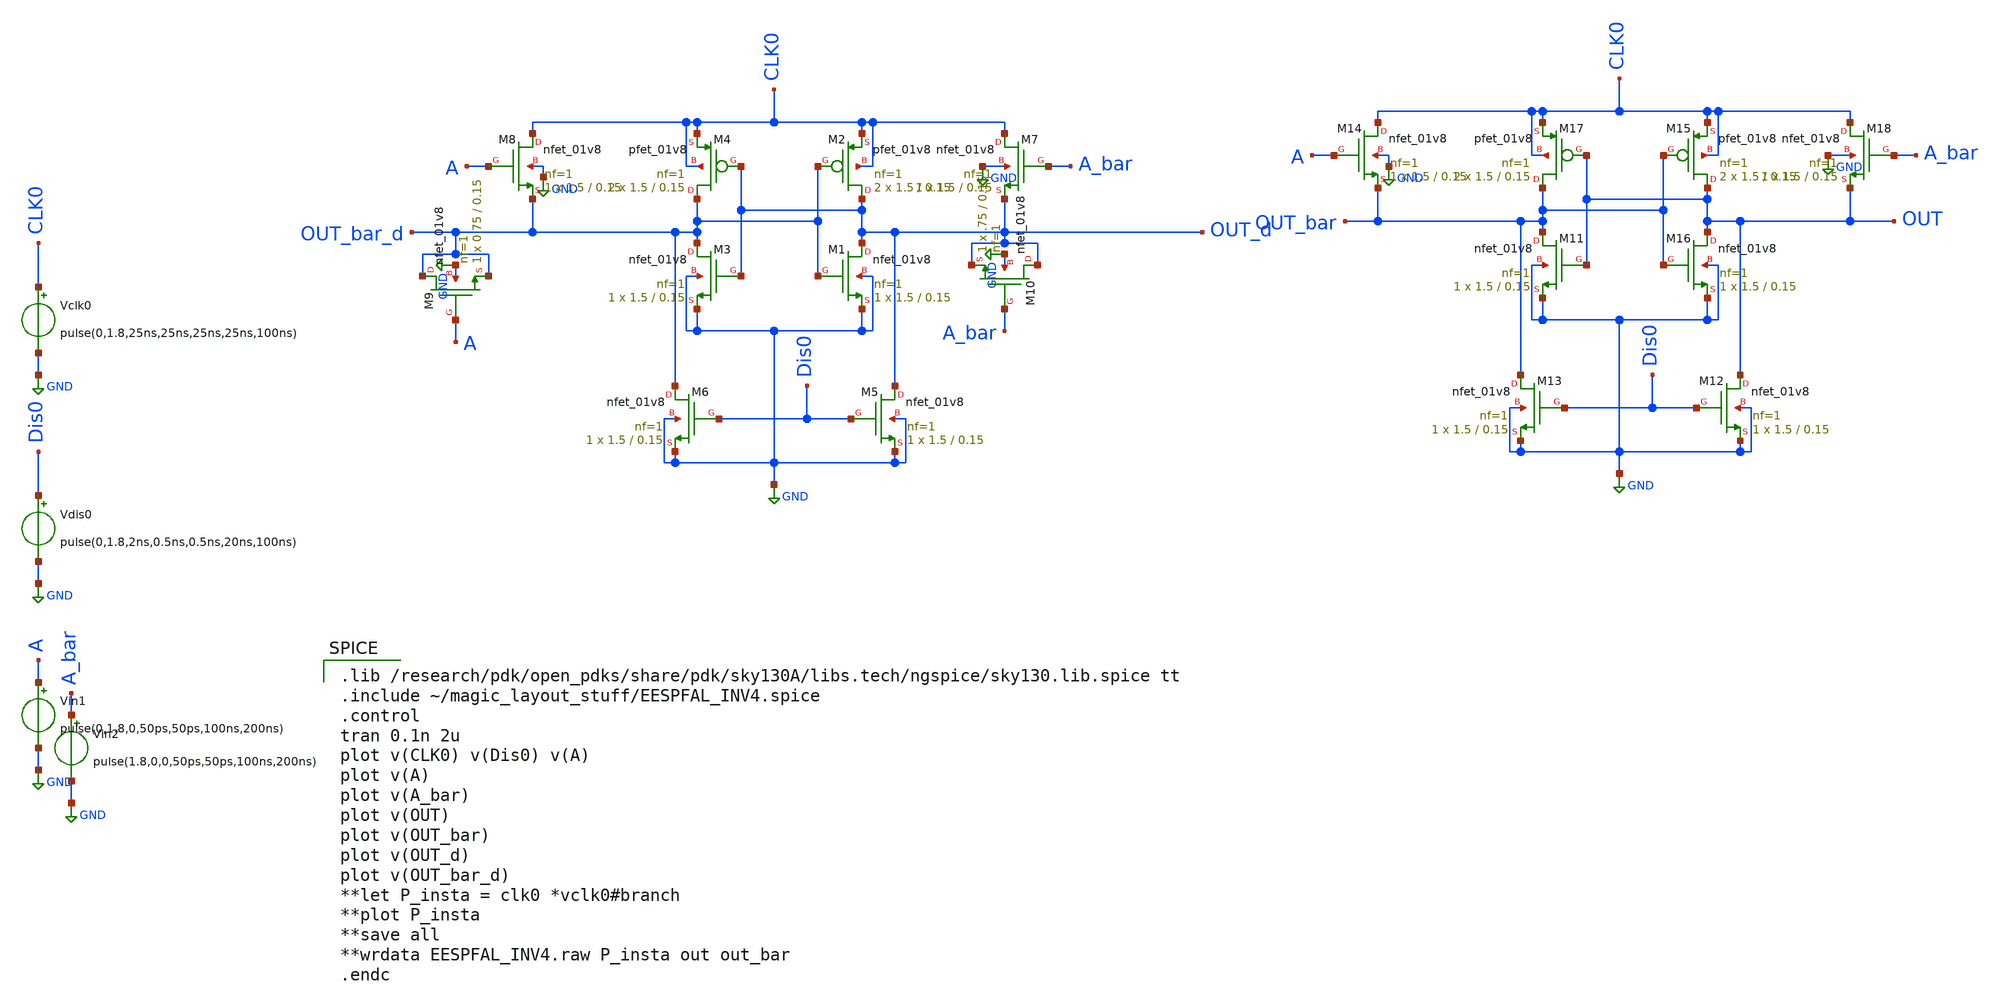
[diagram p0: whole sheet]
** sch_path: skywater_stuff/EESPFAL_INV_sim.sch
**.subckt EESPFAL_INV_sim
Vin2 A_bar GND pulse(1.8,0,0,50ps,50ps,100ns,200ns)
Vdis0 Dis0 GND pulse(0,1.8,2ns,0.5ns,0.5ns,20ns,100ns)
Vin1 A GND pulse(0,1.8,0,50ps,50ps,100ns,200ns)
Vclk0 CLK0 GND pulse(0,1.8,25ns,25ns,25ns,25ns,100ns)
XM7 CLK0 A_bar OUT_d GND sky130_fd_pr__nfet_01v8 L=0.15 W=1.5 nf=1 ad='int((nf+1)/2) * W/nf * 0.29' as='int((nf+2)/2) * W/nf * 0.29'
+ pd='2*int((nf+1)/2) * (W/nf + 0.29)' ps='2*int((nf+2)/2) * (W/nf + 0.29)' nrd='0.29 / W' nrs='0.29 / W'
+ sa=0 sb=0 sd=0 mult=1 m=1
XM3 OUT_bar_d OUT_d GND GND sky130_fd_pr__nfet_01v8 L=0.15 W=1.5 nf=1 ad='int((nf+1)/2) * W/nf * 0.29'
+ as='int((nf+2)/2) * W/nf * 0.29' pd='2*int((nf+1)/2) * (W/nf + 0.29)' ps='2*int((nf+2)/2) * (W/nf + 0.29)'
+ nrd='0.29 / W' nrs='0.29 / W' sa=0 sb=0 sd=0 mult=1 m=1
XM5 OUT_d Dis0 GND GND sky130_fd_pr__nfet_01v8 L=0.15 W=1.5 nf=1 ad='int((nf+1)/2) * W/nf * 0.29' as='int((nf+2)/2) * W/nf * 0.29'
+ pd='2*int((nf+1)/2) * (W/nf + 0.29)' ps='2*int((nf+2)/2) * (W/nf + 0.29)' nrd='0.29 / W' nrs='0.29 / W'
+ sa=0 sb=0 sd=0 mult=1 m=1
XM6 OUT_bar_d Dis0 GND GND sky130_fd_pr__nfet_01v8 L=0.15 W=1.5 nf=1 ad='int((nf+1)/2) * W/nf * 0.29'
+ as='int((nf+2)/2) * W/nf * 0.29' pd='2*int((nf+1)/2) * (W/nf + 0.29)' ps='2*int((nf+2)/2) * (W/nf + 0.29)'
+ nrd='0.29 / W' nrs='0.29 / W' sa=0 sb=0 sd=0 mult=1 m=1
XM8 CLK0 A OUT_bar_d GND sky130_fd_pr__nfet_01v8 L=0.15 W=1.5 nf=1 ad='int((nf+1)/2) * W/nf * 0.29' as='int((nf+2)/2) * W/nf * 0.29'
+ pd='2*int((nf+1)/2) * (W/nf + 0.29)' ps='2*int((nf+2)/2) * (W/nf + 0.29)' nrd='0.29 / W' nrs='0.29 / W'
+ sa=0 sb=0 sd=0 mult=1 m=1
XM2 OUT_d OUT_bar_d CLK0 CLK0 sky130_fd_pr__pfet_01v8 L=0.15 W=1.5 nf=1 ad='int((nf+1)/2) * W/nf * 0.29'
+ as='int((nf+2)/2) * W/nf * 0.29' pd='2*int((nf+1)/2) * (W/nf + 0.29)' ps='2*int((nf+2)/2) * (W/nf + 0.29)'
+ nrd='0.29 / W' nrs='0.29 / W' sa=0 sb=0 sd=0 mult=2 m=2
XM1 OUT_d OUT_bar_d GND GND sky130_fd_pr__nfet_01v8 L=0.15 W=1.5 nf=1 ad='int((nf+1)/2) * W/nf * 0.29'
+ as='int((nf+2)/2) * W/nf * 0.29' pd='2*int((nf+1)/2) * (W/nf + 0.29)' ps='2*int((nf+2)/2) * (W/nf + 0.29)'
+ nrd='0.29 / W' nrs='0.29 / W' sa=0 sb=0 sd=0 mult=1 m=1
XM4 OUT_bar_d OUT_d CLK0 CLK0 sky130_fd_pr__pfet_01v8 L=0.15 W=1.5 nf=1 ad='int((nf+1)/2) * W/nf * 0.29'
+ as='int((nf+2)/2) * W/nf * 0.29' pd='2*int((nf+1)/2) * (W/nf + 0.29)' ps='2*int((nf+2)/2) * (W/nf + 0.29)'
+ nrd='0.29 / W' nrs='0.29 / W' sa=0 sb=0 sd=0 mult=2 m=2
XM11 OUT_bar OUT GND GND sky130_fd_pr__nfet_01v8 L=0.15 W=1.5 nf=1 ad='int((nf+1)/2) * W/nf * 0.29' as='int((nf+2)/2) * W/nf * 0.29'
+ pd='2*int((nf+1)/2) * (W/nf + 0.29)' ps='2*int((nf+2)/2) * (W/nf + 0.29)' nrd='0.29 / W' nrs='0.29 / W'
+ sa=0 sb=0 sd=0 mult=1 m=1
XM12 OUT Dis0 GND GND sky130_fd_pr__nfet_01v8 L=0.15 W=1.5 nf=1 ad='int((nf+1)/2) * W/nf * 0.29' as='int((nf+2)/2) * W/nf * 0.29'
+ pd='2*int((nf+1)/2) * (W/nf + 0.29)' ps='2*int((nf+2)/2) * (W/nf + 0.29)' nrd='0.29 / W' nrs='0.29 / W'
+ sa=0 sb=0 sd=0 mult=1 m=1
XM13 OUT_bar Dis0 GND GND sky130_fd_pr__nfet_01v8 L=0.15 W=1.5 nf=1 ad='int((nf+1)/2) * W/nf * 0.29'
+ as='int((nf+2)/2) * W/nf * 0.29' pd='2*int((nf+1)/2) * (W/nf + 0.29)' ps='2*int((nf+2)/2) * (W/nf + 0.29)'
+ nrd='0.29 / W' nrs='0.29 / W' sa=0 sb=0 sd=0 mult=1 m=1
XM14 CLK0 A OUT_bar GND sky130_fd_pr__nfet_01v8 L=0.15 W=1.5 nf=1 ad='int((nf+1)/2) * W/nf * 0.29' as='int((nf+2)/2) * W/nf * 0.29'
+ pd='2*int((nf+1)/2) * (W/nf + 0.29)' ps='2*int((nf+2)/2) * (W/nf + 0.29)' nrd='0.29 / W' nrs='0.29 / W'
+ sa=0 sb=0 sd=0 mult=1 m=1
XM15 OUT OUT_bar CLK0 CLK0 sky130_fd_pr__pfet_01v8 L=0.15 W=1.5 nf=1 ad='int((nf+1)/2) * W/nf * 0.29'
+ as='int((nf+2)/2) * W/nf * 0.29' pd='2*int((nf+1)/2) * (W/nf + 0.29)' ps='2*int((nf+2)/2) * (W/nf + 0.29)'
+ nrd='0.29 / W' nrs='0.29 / W' sa=0 sb=0 sd=0 mult=2 m=2
XM16 OUT OUT_bar GND GND sky130_fd_pr__nfet_01v8 L=0.15 W=1.5 nf=1 ad='int((nf+1)/2) * W/nf * 0.29' as='int((nf+2)/2) * W/nf * 0.29'
+ pd='2*int((nf+1)/2) * (W/nf + 0.29)' ps='2*int((nf+2)/2) * (W/nf + 0.29)' nrd='0.29 / W' nrs='0.29 / W'
+ sa=0 sb=0 sd=0 mult=1 m=1
XM17 OUT_bar OUT CLK0 CLK0 sky130_fd_pr__pfet_01v8 L=0.15 W=1.5 nf=1 ad='int((nf+1)/2) * W/nf * 0.29'
+ as='int((nf+2)/2) * W/nf * 0.29' pd='2*int((nf+1)/2) * (W/nf + 0.29)' ps='2*int((nf+2)/2) * (W/nf + 0.29)'
+ nrd='0.29 / W' nrs='0.29 / W' sa=0 sb=0 sd=0 mult=2 m=2
XM18 CLK0 A_bar OUT GND sky130_fd_pr__nfet_01v8 L=0.15 W=1.5 nf=1 ad='int((nf+1)/2) * W/nf * 0.29' as='int((nf+2)/2) * W/nf * 0.29'
+ pd='2*int((nf+1)/2) * (W/nf + 0.29)' ps='2*int((nf+2)/2) * (W/nf + 0.29)' nrd='0.29 / W' nrs='0.29 / W'
+ sa=0 sb=0 sd=0 mult=1 m=1
XM9 OUT_bar_d A OUT_bar_d GND sky130_fd_pr__nfet_01v8 L=0.15 W=0.75 nf=1 ad='int((nf+1)/2) * W/nf * 0.29'
+ as='int((nf+2)/2) * W/nf * 0.29' pd='2*int((nf+1)/2) * (W/nf + 0.29)' ps='2*int((nf+2)/2) * (W/nf + 0.29)'
+ nrd='0.29 / W' nrs='0.29 / W' sa=0 sb=0 sd=0 mult=1 m=1
XM10 OUT_d A_bar OUT_d GND sky130_fd_pr__nfet_01v8 L=0.15 W=.75 nf=1 ad='int((nf+1)/2) * W/nf * 0.29'
+ as='int((nf+2)/2) * W/nf * 0.29' pd='2*int((nf+1)/2) * (W/nf + 0.29)' ps='2*int((nf+2)/2) * (W/nf + 0.29)'
+ nrd='0.29 / W' nrs='0.29 / W' sa=0 sb=0 sd=0 mult=1 m=1
**** begin user architecture code

.lib /research/pdk/open_pdks/share/pdk/sky130A/libs.tech/ngspice/sky130.lib.spice tt
.include ~/magic_layout_stuff/EESPFAL_INV4.spice
.control
tran 0.1n 2u
plot v(CLK0) v(Dis0) v(A)
plot v(A)
plot v(A_bar)
plot v(OUT)
plot v(OUT_bar)
plot v(OUT_d)
plot v(OUT_bar_d)
**let P_insta = clk0 *vclk0#branch
**plot P_insta
**save all
**wrdata EESPFAL_INV4.raw P_insta out out_bar
.endc


**** end user architecture code
**.ends
.GLOBAL GND
.end
